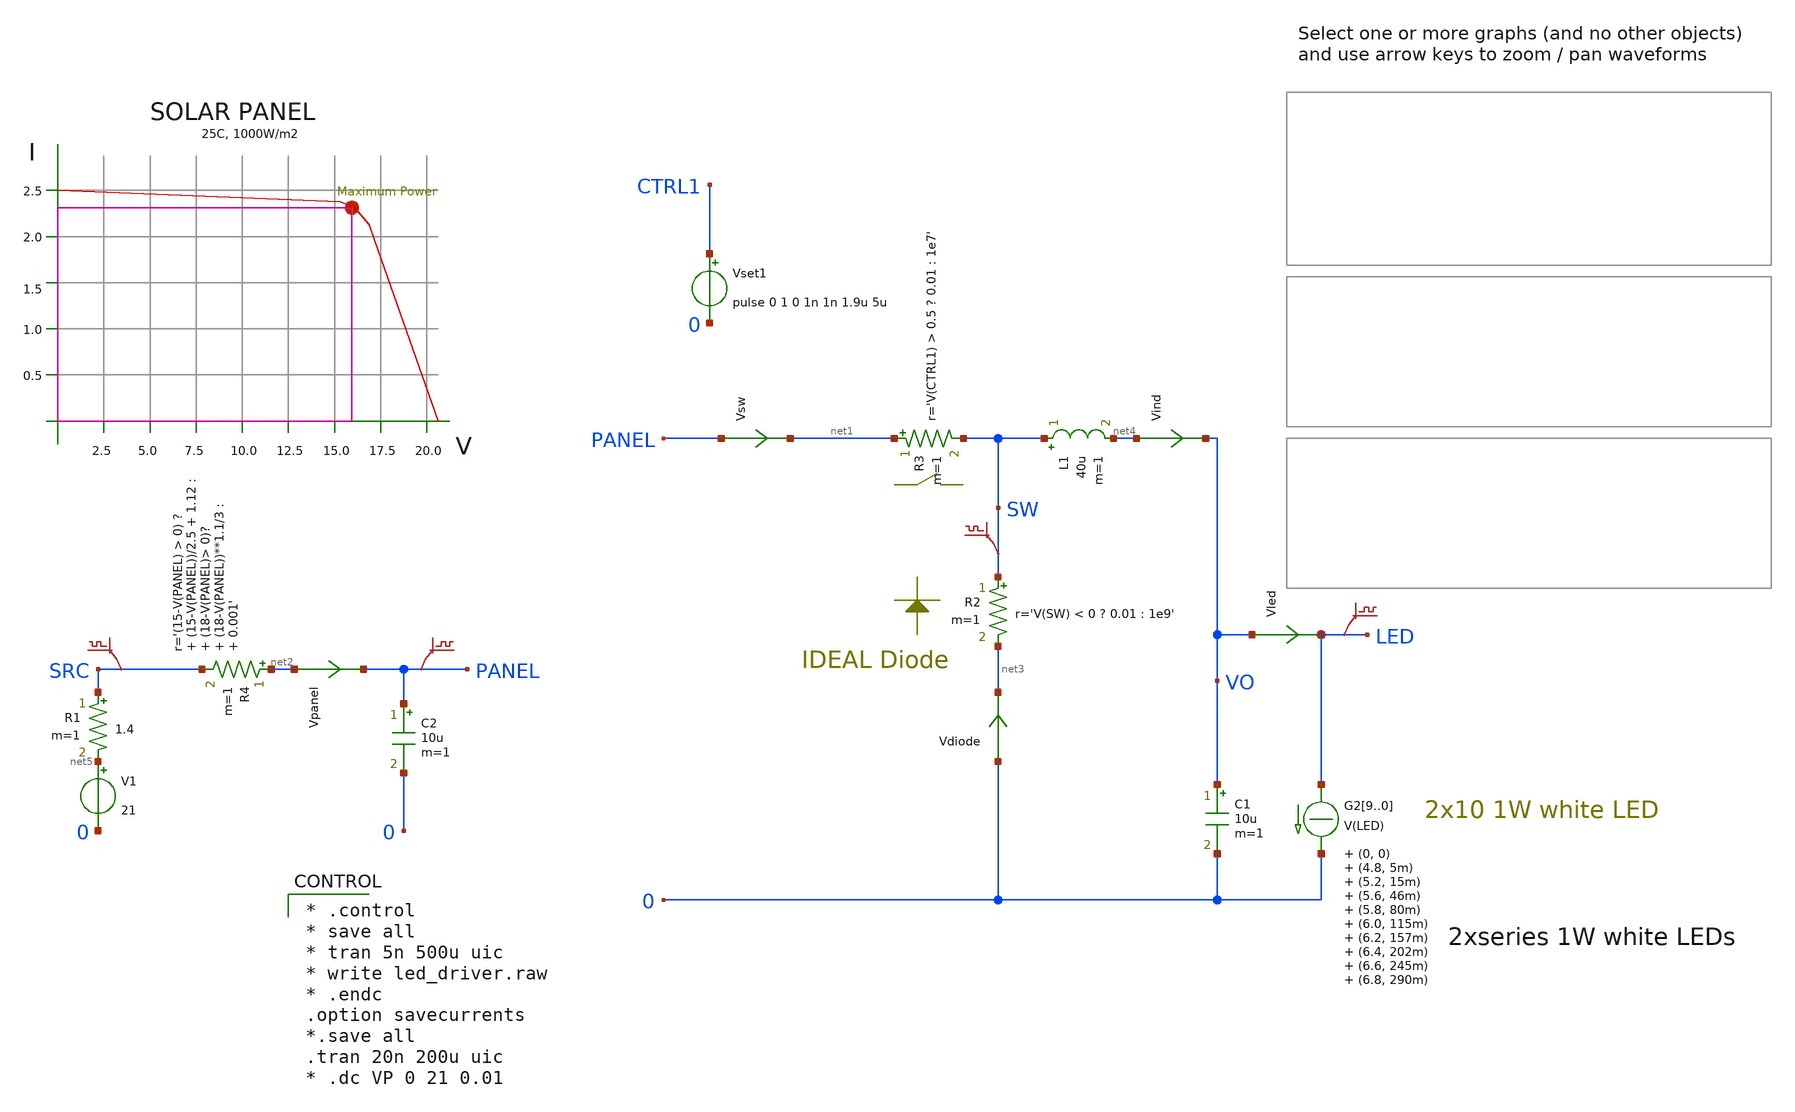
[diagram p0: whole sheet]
** sch_path: xschem_library/ngspice/solar_panel.sch
**.subckt solar_panel
V1 net5 0 21
R1 SRC net5 1.4 m=1
Vled VO LED 0
.save i(vled)
L1 SW net4 40u m=1
C1 VO 0 10u m=1
Vpanel net2 PANEL 0
.save i(vpanel)
R2 SW net3 r='V(SW) < 0 ? 0.01 : 1e9' m=1
Vset1 CTRL1 0 pulse 0 1 0 1n 1n 1.9u 5u
R3 net1 SW r='V(CTRL1) > 0.5 ? 0.01 : 1e7' m=1
R4 net2 SRC r='(15-V(PANEL) > 0) ? (15-V(PANEL))/2.5 + 1.12 : (18-V(PANEL)> 0)? (18-V(PANEL))**1.1/3 : 0.001'
+ m=1
Vind net4 VO 0
.save i(vind)
C2 PANEL 0 10u m=1
G29 LED 0 TABLE { V(LED) } = (0, 0) (4.8, 5m) (5.2, 15m) (5.6, 46m) (5.8, 80m) (6.0, 115m) (6.2, 157m)
+ (6.4, 202m) (6.6, 245m) (6.8, 290m) (7.0, 337m) (7.2, 395m) (7.4, 470m) (8.0, 750m)
G28 LED 0 TABLE { V(LED) } = (0, 0) (4.8, 5m) (5.2, 15m) (5.6, 46m) (5.8, 80m) (6.0, 115m) (6.2, 157m)
+ (6.4, 202m) (6.6, 245m) (6.8, 290m) (7.0, 337m) (7.2, 395m) (7.4, 470m) (8.0, 750m)
G27 LED 0 TABLE { V(LED) } = (0, 0) (4.8, 5m) (5.2, 15m) (5.6, 46m) (5.8, 80m) (6.0, 115m) (6.2, 157m)
+ (6.4, 202m) (6.6, 245m) (6.8, 290m) (7.0, 337m) (7.2, 395m) (7.4, 470m) (8.0, 750m)
G26 LED 0 TABLE { V(LED) } = (0, 0) (4.8, 5m) (5.2, 15m) (5.6, 46m) (5.8, 80m) (6.0, 115m) (6.2, 157m)
+ (6.4, 202m) (6.6, 245m) (6.8, 290m) (7.0, 337m) (7.2, 395m) (7.4, 470m) (8.0, 750m)
G25 LED 0 TABLE { V(LED) } = (0, 0) (4.8, 5m) (5.2, 15m) (5.6, 46m) (5.8, 80m) (6.0, 115m) (6.2, 157m)
+ (6.4, 202m) (6.6, 245m) (6.8, 290m) (7.0, 337m) (7.2, 395m) (7.4, 470m) (8.0, 750m)
G24 LED 0 TABLE { V(LED) } = (0, 0) (4.8, 5m) (5.2, 15m) (5.6, 46m) (5.8, 80m) (6.0, 115m) (6.2, 157m)
+ (6.4, 202m) (6.6, 245m) (6.8, 290m) (7.0, 337m) (7.2, 395m) (7.4, 470m) (8.0, 750m)
G23 LED 0 TABLE { V(LED) } = (0, 0) (4.8, 5m) (5.2, 15m) (5.6, 46m) (5.8, 80m) (6.0, 115m) (6.2, 157m)
+ (6.4, 202m) (6.6, 245m) (6.8, 290m) (7.0, 337m) (7.2, 395m) (7.4, 470m) (8.0, 750m)
G22 LED 0 TABLE { V(LED) } = (0, 0) (4.8, 5m) (5.2, 15m) (5.6, 46m) (5.8, 80m) (6.0, 115m) (6.2, 157m)
+ (6.4, 202m) (6.6, 245m) (6.8, 290m) (7.0, 337m) (7.2, 395m) (7.4, 470m) (8.0, 750m)
G21 LED 0 TABLE { V(LED) } = (0, 0) (4.8, 5m) (5.2, 15m) (5.6, 46m) (5.8, 80m) (6.0, 115m) (6.2, 157m)
+ (6.4, 202m) (6.6, 245m) (6.8, 290m) (7.0, 337m) (7.2, 395m) (7.4, 470m) (8.0, 750m)
G20 LED 0 TABLE { V(LED) } = (0, 0) (4.8, 5m) (5.2, 15m) (5.6, 46m) (5.8, 80m) (6.0, 115m) (6.2, 157m)
+ (6.4, 202m) (6.6, 245m) (6.8, 290m) (7.0, 337m) (7.2, 395m) (7.4, 470m) (8.0, 750m)
Vsw PANEL net1 0
.save i(vsw)
Vdiode 0 net3 0
.save i(vdiode)
.save v(led)
.save v(panel)
.save v(sw)
.save v(src)
**** begin user architecture code

* .control
* save all
* tran 5n 500u uic
* write led_driver.raw
* .endc
.option savecurrents
*.save all
.tran 20n 200u uic
* .dc VP 0 21 0.01



.MODEL DIODE D(IS=1.139e-08 RS=0.99 CJO=9.3e-12 VJ=1.6 M=0.411 BV=30 EG=0.7 )
.MODEL swmod SW(VT=0.1 VH=0.01 RON=0.01 ROFF=10000000)


**** end user architecture code
**.ends
.end
